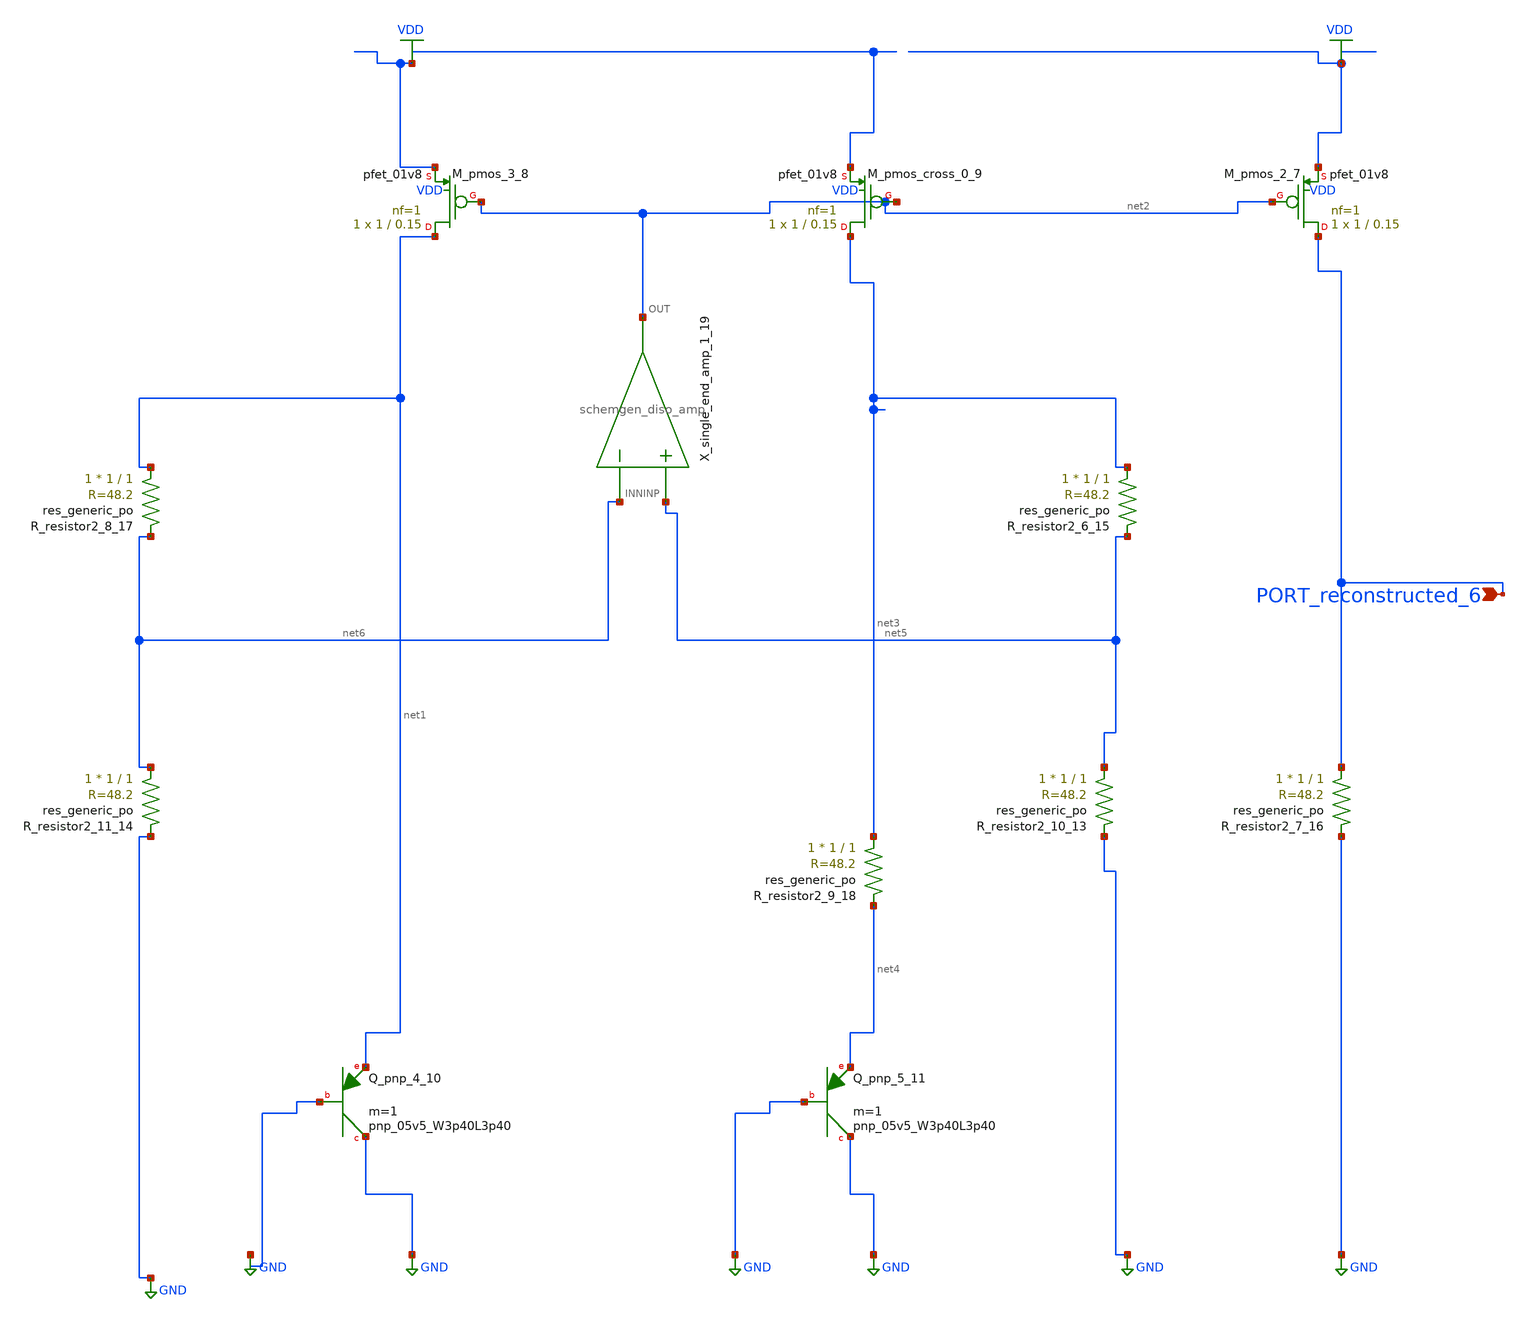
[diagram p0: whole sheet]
** sch_path: schematics/Image2Net/017.sch
**.subckt 017 PORT_reconstructed_6
*.ipin PORT_reconstructed_6
XM_pmos_2_7 PORT_reconstructed_6 net2 VDD VDD sky130_fd_pr__pfet_01v8 L=0.15 W=1 nf=1 ad='int((1 + 1)/2) * 1 / 1 * 0.29'
+ as='int((1 + 2)/2) * 1 / 1 * 0.29' pd='2*int((1 + 1)/2) * (1 / 1 + 0.29)' ps='2*int((1 + 2)/2) * (1 / 1 + 0.29)'
+ nrd='0.29 / 1 ' nrs='0.29 / 1 ' sa=0 sb=0 sd=0 mult=1 m=1
XM_pmos_3_8 net1 net2 VDD VDD sky130_fd_pr__pfet_01v8 L=0.15 W=1 nf=1 ad='int((1 + 1)/2) * 1 / 1 * 0.29'
+ as='int((1 + 2)/2) * 1 / 1 * 0.29' pd='2*int((1 + 1)/2) * (1 / 1 + 0.29)' ps='2*int((1 + 2)/2) * (1 / 1 + 0.29)'
+ nrd='0.29 / 1 ' nrs='0.29 / 1 ' sa=0 sb=0 sd=0 mult=1 m=1
XM_pmos_cross_0_9 net3 net2 VDD VDD sky130_fd_pr__pfet_01v8 L=0.15 W=1 nf=1 ad='int((1 + 1)/2) * 1 / 1 * 0.29'
+ as='int((1 + 2)/2) * 1 / 1 * 0.29' pd='2*int((1 + 1)/2) * (1 / 1 + 0.29)' ps='2*int((1 + 2)/2) * (1 / 1 + 0.29)'
+ nrd='0.29 / 1 ' nrs='0.29 / 1 ' sa=0 sb=0 sd=0 mult=1 m=1
XQ_pnp_4_10 GND GND net1 sky130_fd_pr__pnp_05v5_W3p40L3p40 m=1
XQ_pnp_5_11 GND GND net4 sky130_fd_pr__pnp_05v5_W3p40L3p40 m=1
XR_resistor2_10_13 net5 GND sky130_fd_pr__res_generic_po W=1 L=1 m=1
XR_resistor2_11_14 net6 GND sky130_fd_pr__res_generic_po W=1 L=1 m=1
XR_resistor2_6_15 net3 net5 sky130_fd_pr__res_generic_po W=1 L=1 m=1
XR_resistor2_7_16 PORT_reconstructed_6 GND sky130_fd_pr__res_generic_po W=1 L=1 m=1
XR_resistor2_8_17 net1 net6 sky130_fd_pr__res_generic_po W=1 L=1 m=1
XR_resistor2_9_18 net3 net4 sky130_fd_pr__res_generic_po W=1 L=1 m=1
X_single_end_amp_1_19 net5 net6 net2 schemgen_diso_amp
**.ends

* expanding   symbol:  schemgen_diso_amp.sym # of pins=3
** sym_path: symbols/schemgen_diso_amp.sym
.subckt schemgen_diso_amp INP INN OUT
* SchemGen ideal op-amp: Vout = 1e5 * (V(INP) - V(INN))
E1 OUT 0 INP INN 1e5
.ends schemgen_diso_amp
.GLOBAL GND
.GLOBAL VDD
.end
